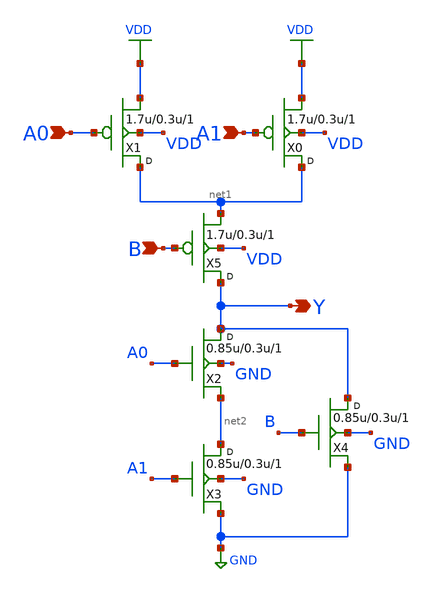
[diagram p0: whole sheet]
** sch_path: gf180mcu_osu_sc_gp9t3v3/cells/aoi21/gf180mcu_osu_sc_gp9t3v3__aoi21_1.sch
**.subckt gf180mcu_osu_sc_gp9t3v3__aoi21_1 A0 A1 Y B
*.ipin A0
*.ipin A1
*.opin Y
*.ipin B
X1 net1 A0 VDD VDD pfet_03p3 w=1.7u l=0.3u m=1
X0 net1 A1 VDD VDD pfet_03p3 w=1.7u l=0.3u m=1
X2 Y A0 net2 GND nfet_03p3 w=0.85u l=0.3u m=1
X3 net2 A1 GND GND nfet_03p3 w=0.85u l=0.3u m=1
X4 Y B GND GND nfet_03p3 w=0.85u l=0.3u m=1
X5 Y B net1 VDD pfet_03p3 w=1.7u l=0.3u m=1
**.ends
.GLOBAL VDD
.GLOBAL GND
.end
